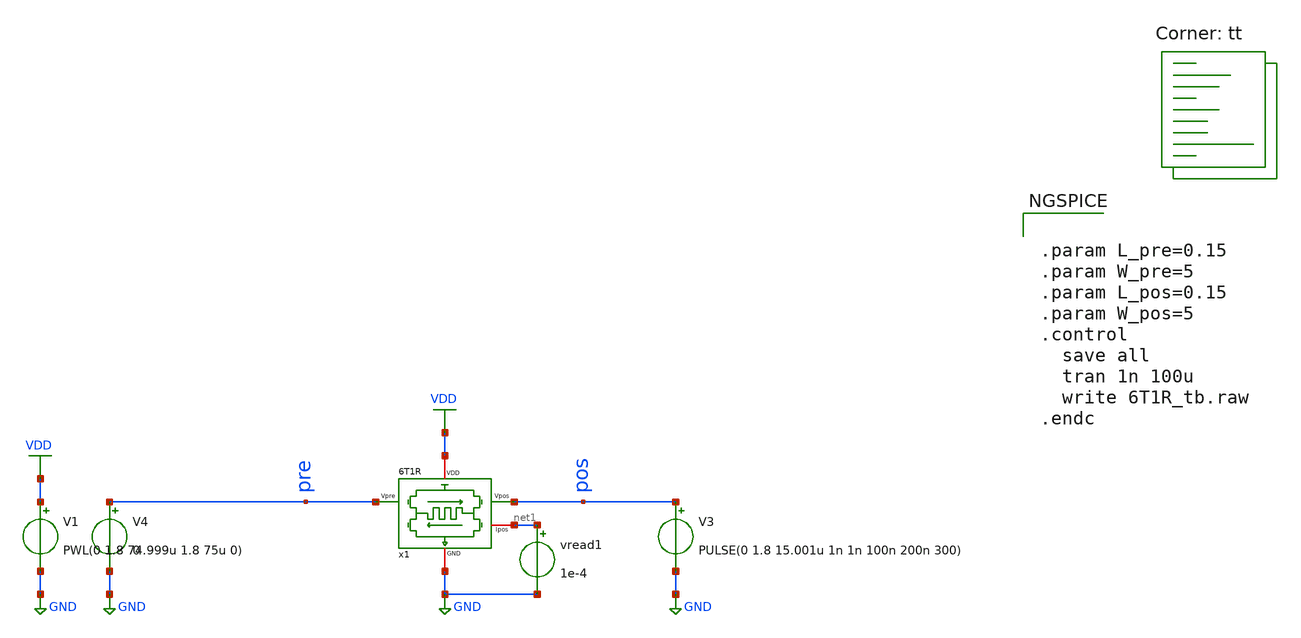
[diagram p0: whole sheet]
** sch_path: synapse/6T1R_tb.sch
**.subckt 6T1R_tb
V1 VDD GND PWL(0 1.8 74.999u 1.8 75u 0)
V3 pos GND PULSE(0 1.8 15.001u 1n 1n 100n 200n 300)
vread1 net1 GND 1e-4
x1 VDD net1 pre pos GND 6T1R
V4 pre GND 0
**** begin user architecture code
.lib $::SKYWATER_MODELS/sky130.lib.spice tt

** opencircuitdesign pdks install
.inc $::SKYWATER_MODELS/rram_v2.spice



.param L_pre=0.15
.param W_pre=5
.param L_pos=0.15
.param W_pos=5
.control
  save all
  tran 1n 100u
  write 6T1R_tb.raw
.endc


**** end user architecture code
**.ends
.GLOBAL GND
.GLOBAL VDD
.end
